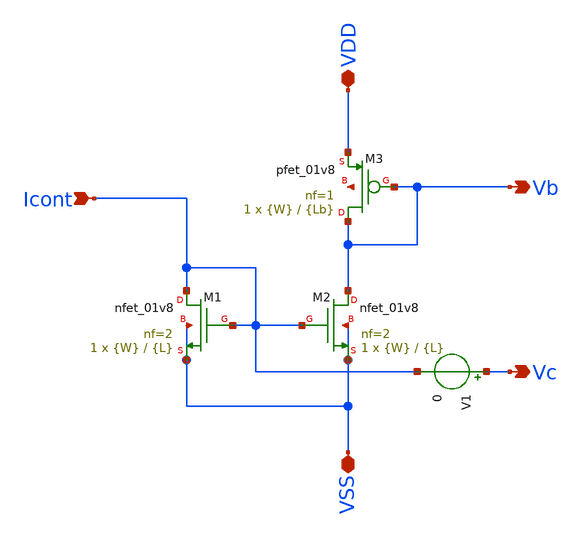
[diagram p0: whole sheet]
** sch_path: xschem/vco_bias_p.sch
**.subckt vco_bias_p VDD VSS Icont Vb Vc
*.iopin VDD
*.iopin VSS
*.ipin Icont
*.opin Vb
*.opin Vc
XM1 Icont Icont VSS VSS sky130_fd_pr__nfet_01v8 L={L} W={W} nf=2 ad='int((nf+1)/2) * W/nf * 0.29' as='int((nf+2)/2) * W/nf * 0.29'
+ pd='2*int((nf+1)/2) * (W/nf + 0.29)' ps='2*int((nf+2)/2) * (W/nf + 0.29)' nrd='0.29 / W' nrs='0.29 / W'
+ sa=0 sb=0 sd=0 mult=1 m=1
XM2 Vb Icont VSS VSS sky130_fd_pr__nfet_01v8 L={L} W={W} nf=2 ad='int((nf+1)/2) * W/nf * 0.29' as='int((nf+2)/2) * W/nf * 0.29'
+ pd='2*int((nf+1)/2) * (W/nf + 0.29)' ps='2*int((nf+2)/2) * (W/nf + 0.29)' nrd='0.29 / W' nrs='0.29 / W'
+ sa=0 sb=0 sd=0 mult=1 m=1
V1 Vc Icont 0
XM3 Vb Vb VDD net1 sky130_fd_pr__pfet_01v8 L={Lb} W={W} nf=1 ad='int((nf+1)/2) * W/nf * 0.29' as='int((nf+2)/2) * W/nf * 0.29'
+ pd='2*int((nf+1)/2) * (W/nf + 0.29)' ps='2*int((nf+2)/2) * (W/nf + 0.29)' nrd='0.29 / W' nrs='0.29 / W'
+ sa=0 sb=0 sd=0 mult=1 m=1
**.ends
.end
